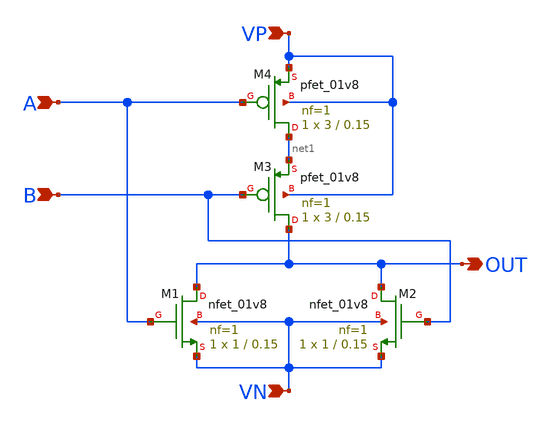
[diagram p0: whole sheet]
** sch_path: basic_cell/single_cell/nor/nor.sch
**.subckt nor A B VP VN OUT
*.ipin A
*.ipin B
*.ipin VP
*.ipin VN
*.opin OUT
XM1 OUT A VN VN sky130_fd_pr__nfet_01v8 L=0.15 W=1 nf=1 ad='int((nf+1)/2) * W/nf * 0.29' as='int((nf+2)/2) * W/nf * 0.29'
+ pd='2*int((nf+1)/2) * (W/nf + 0.29)' ps='2*int((nf+2)/2) * (W/nf + 0.29)' nrd='0.29 / W' nrs='0.29 / W'
+ sa=0 sb=0 sd=0 mult=1 m=1
XM2 OUT B VN VN sky130_fd_pr__nfet_01v8 L=0.15 W=1 nf=1 ad='int((nf+1)/2) * W/nf * 0.29' as='int((nf+2)/2) * W/nf * 0.29'
+ pd='2*int((nf+1)/2) * (W/nf + 0.29)' ps='2*int((nf+2)/2) * (W/nf + 0.29)' nrd='0.29 / W' nrs='0.29 / W'
+ sa=0 sb=0 sd=0 mult=1 m=1
XM3 OUT B net1 VP sky130_fd_pr__pfet_01v8 L=0.15 W=3 nf=1 ad='int((nf+1)/2) * W/nf * 0.29' as='int((nf+2)/2) * W/nf * 0.29'
+ pd='2*int((nf+1)/2) * (W/nf + 0.29)' ps='2*int((nf+2)/2) * (W/nf + 0.29)' nrd='0.29 / W' nrs='0.29 / W'
+ sa=0 sb=0 sd=0 mult=1 m=1
XM4 net1 A VP VP sky130_fd_pr__pfet_01v8 L=0.15 W=3 nf=1 ad='int((nf+1)/2) * W/nf * 0.29' as='int((nf+2)/2) * W/nf * 0.29'
+ pd='2*int((nf+1)/2) * (W/nf + 0.29)' ps='2*int((nf+2)/2) * (W/nf + 0.29)' nrd='0.29 / W' nrs='0.29 / W'
+ sa=0 sb=0 sd=0 mult=1 m=1
**.ends
.end
